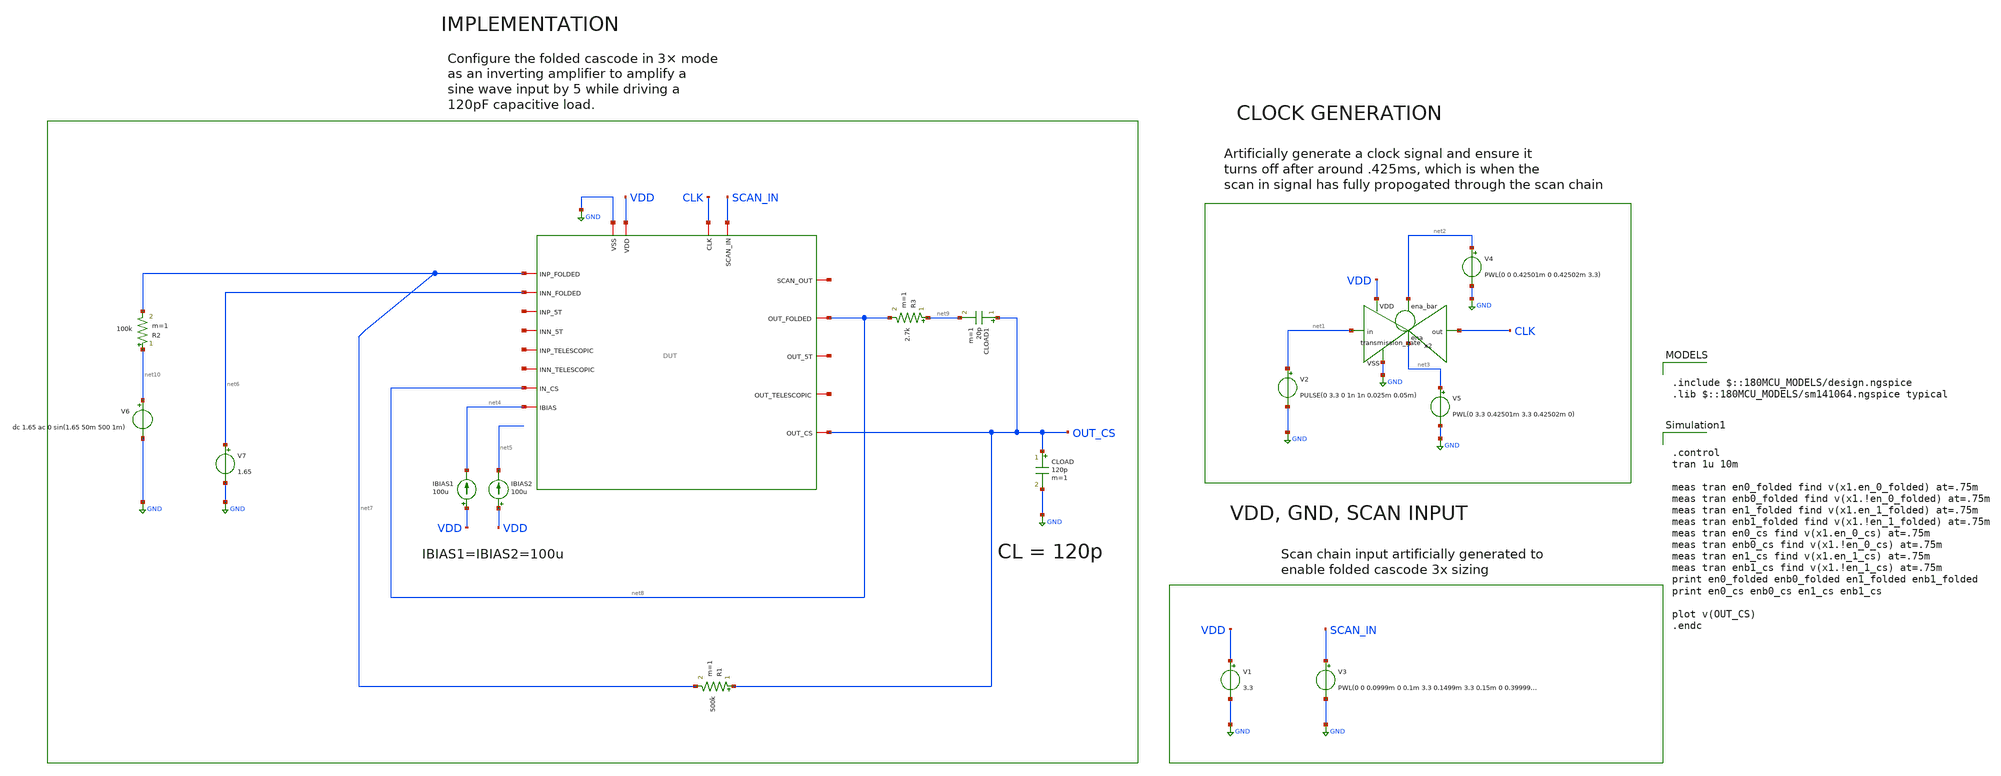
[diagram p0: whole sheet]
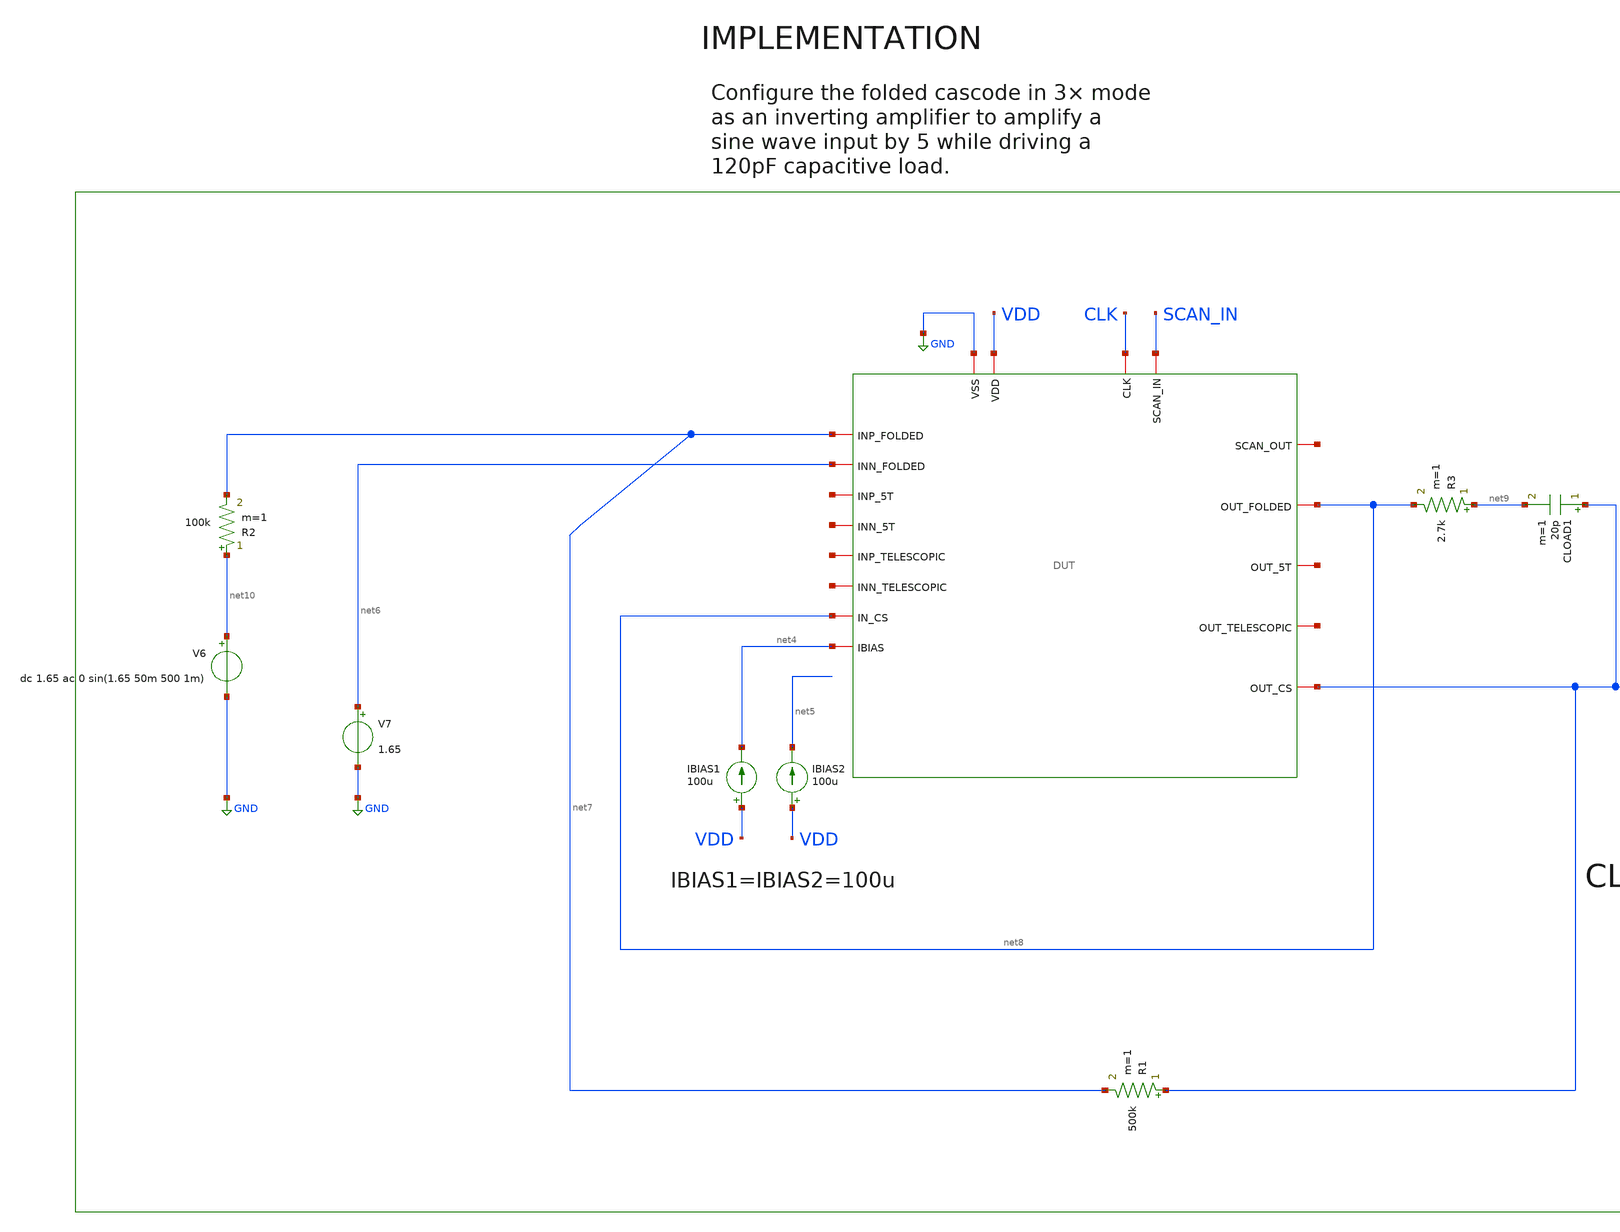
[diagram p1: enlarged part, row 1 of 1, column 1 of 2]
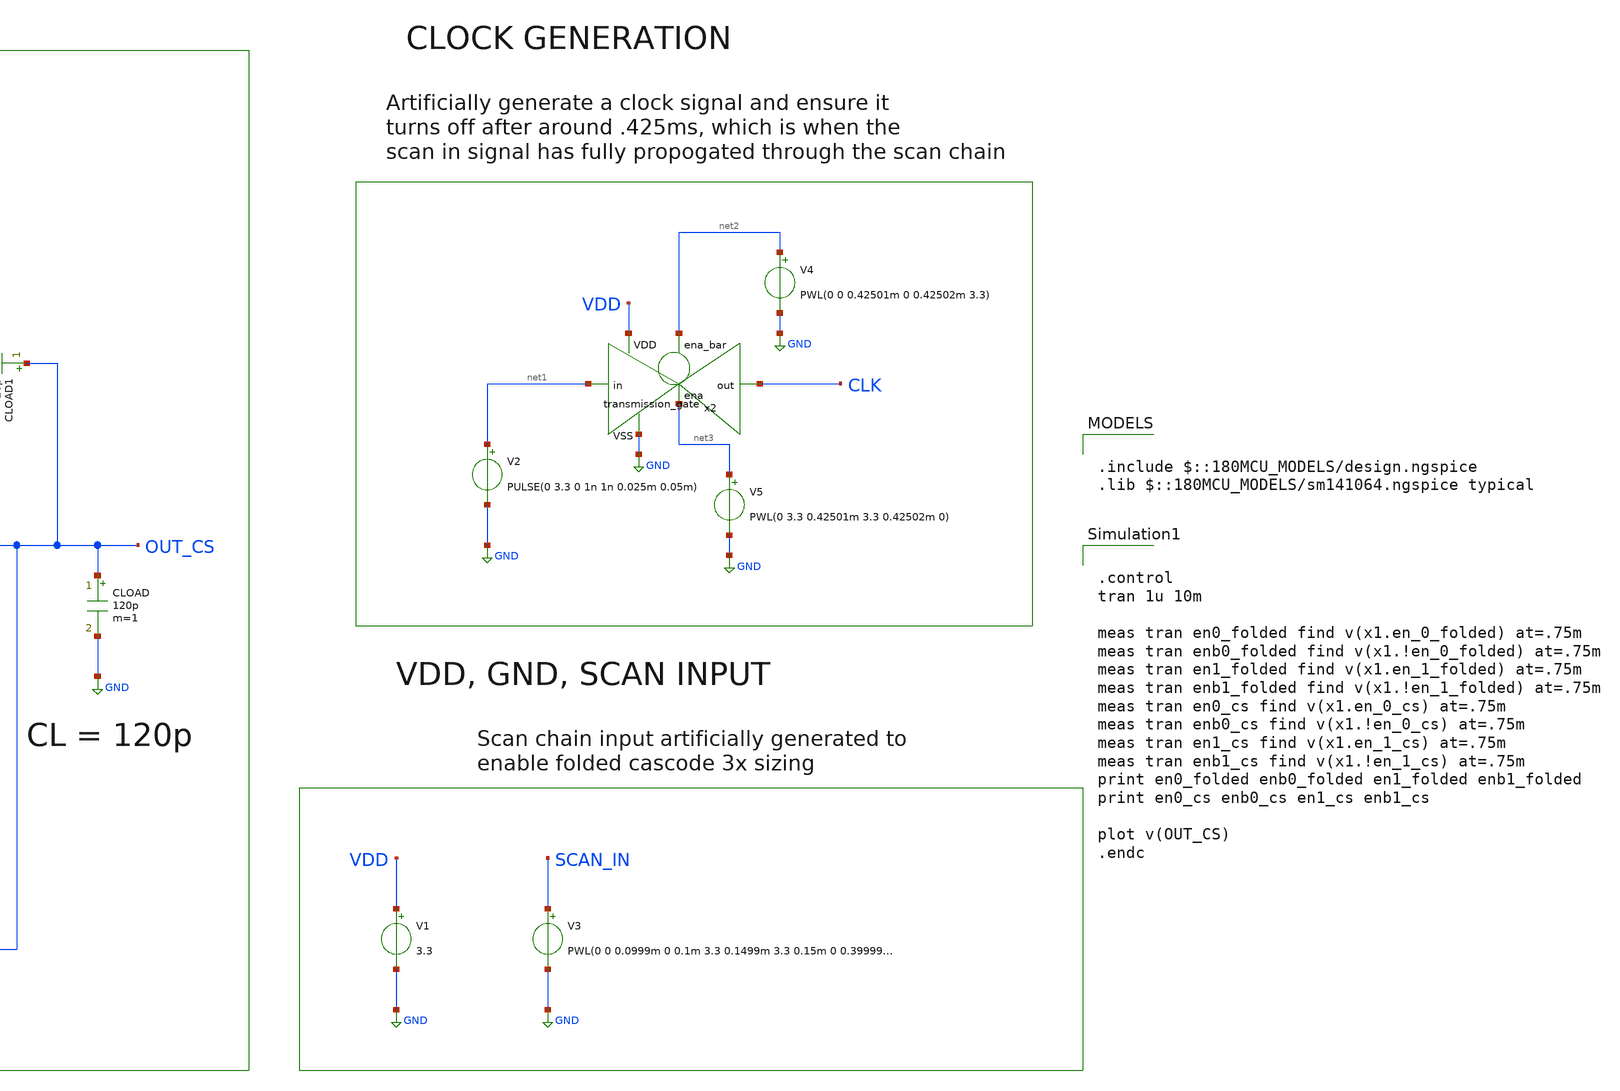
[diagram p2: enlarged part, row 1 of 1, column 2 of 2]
** sch_path: designs/untitled.sch
**.subckt untitled
V3 SCAN_IN GND PWL(0 0 0.0999m 0 0.1m 3.3 0.1499m 3.3 0.15m 0 0.39999m 0 0.4m 3.3 0.499999m 3.3 0.5m
+ 0)
V1 VDD GND 3.3
V2 net1 GND PULSE(0 3.3 0 1n 1n 0.025m 0.05m)
x2 net2 VDD CLK net1 GND net3 transmission_gate
V4 net2 GND PWL(0 0 0.42501m 0 0.42502m 3.3)
V5 net3 GND PWL(0 3.3 0.42501m 3.3 0.42502m 0)
IBIAS1 VDD net4 100u
IBIAS2 VDD net5 100u
CLOAD OUT_CS GND 120p m=1
R3 net9 net8 2.7k m=1
CLOAD1 OUT_CS net9 20p m=1
V7 net6 GND 1.65
x1 CLK net11 SCAN_IN GND VDD net8 net7 net12 net4 net6 net13 net14 net15 net16 OUT_CS net8 net17 DUT
R2 net10 net7 100k m=1
R1 OUT_CS net7 500k m=1
V6 net10 GND dc 1.65 ac 0 sin(1.65 50m 500 1m)
**** begin user architecture code

.include $::180MCU_MODELS/design.ngspice
.lib $::180MCU_MODELS/sm141064.ngspice typical



.control
tran 1u 10m

meas tran en0_folded find v(x1.en_0_folded) at=.75m
meas tran enb0_folded find v(x1.!en_0_folded) at=.75m
meas tran en1_folded find v(x1.en_1_folded) at=.75m
meas tran enb1_folded find v(x1.!en_1_folded) at=.75m
meas tran en0_cs find v(x1.en_0_cs) at=.75m
meas tran enb0_cs find v(x1.!en_0_cs) at=.75m
meas tran en1_cs find v(x1.en_1_cs) at=.75m
meas tran enb1_cs find v(x1.!en_1_cs) at=.75m
print en0_folded enb0_folded en1_folded enb1_folded
print en0_cs enb0_cs en1_cs enb1_cs

plot v(OUT_CS)
.endc


**** end user architecture code
**.ends
.GLOBAL GND
.end
